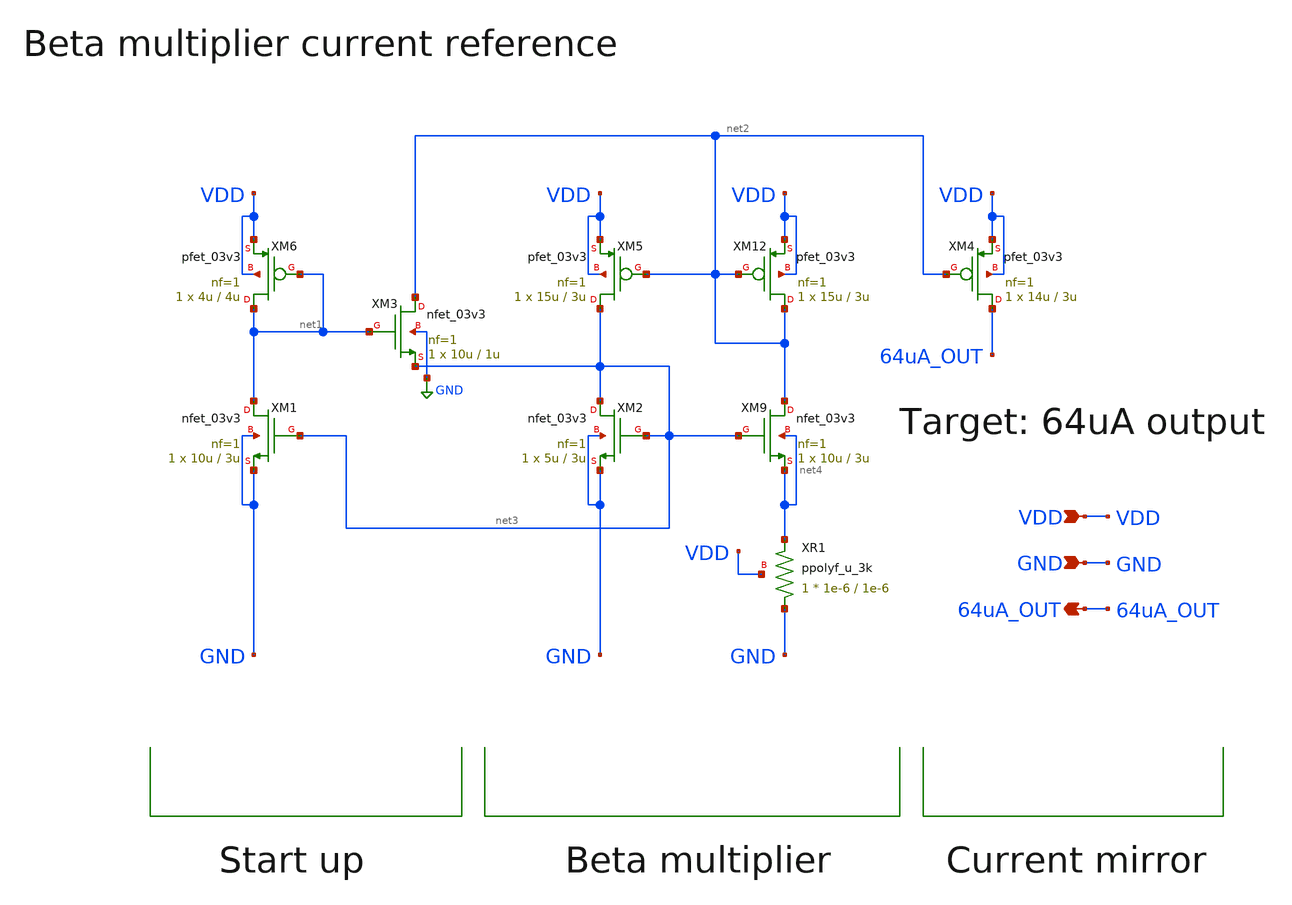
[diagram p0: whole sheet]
** sch_path: designs/libs/core_analog/bmr/bmr.sch
* Copyright 2022 GlobalFoundries PDK Authors
* Licensed under the Apache License, Version 2.0 (the "License");
* you may not use this file except in compliance with the License.
* You may obtain a copy of the License at
* https://www.apache.org/licenses/LICENSE-2.0
* Unless required by applicable law or agreed to in writing, software
* distributed under the License is distributed on an "AS IS" BASIS,
* WITHOUT WARRANTIES OR CONDITIONS OF ANY KIND, either express or implied.
* See the License for the specific language governing permissions and
* limitations under the License.
**.subckt bmr VDD GND 64uA_OUT
*.ipin VDD
*.ipin GND
*.opin 64uA_OUT
XM3 net2 net1 net3 GND nfet_03v3 L=1u W=10u nf=1 ad='int((nf+1)/2) * W/nf * 0.18u' as='int((nf+2)/2) * W/nf * 0.18u'
+ pd='2*int((nf+1)/2) * (W/nf + 0.18u)' ps='2*int((nf+2)/2) * (W/nf + 0.18u)' nrd='0.18u / W' nrs='0.18u / W'
+ sa=0 sb=0 sd=0 m=1
XM5 net3 net2 VDD VDD pfet_03v3 L=3u W=15u nf=1 ad='int((nf+1)/2) * W/nf * 0.18u' as='int((nf+2)/2) * W/nf * 0.18u'
+ pd='2*int((nf+1)/2) * (W/nf + 0.18u)' ps='2*int((nf+2)/2) * (W/nf + 0.18u)' nrd='0.18u / W' nrs='0.18u / W'
+ sa=0 sb=0 sd=0 m=1
XM6 net1 net1 VDD VDD pfet_03v3 L=4u W=4u nf=1 ad='int((nf+1)/2) * W/nf * 0.18u' as='int((nf+2)/2) * W/nf * 0.18u'
+ pd='2*int((nf+1)/2) * (W/nf + 0.18u)' ps='2*int((nf+2)/2) * (W/nf + 0.18u)' nrd='0.18u / W' nrs='0.18u / W'
+ sa=0 sb=0 sd=0 m=1
XM9 net2 net3 net4 net4 nfet_03v3 L=3u W=10u nf=1 ad='int((nf+1)/2) * W/nf * 0.18u' as='int((nf+2)/2) * W/nf * 0.18u'
+ pd='2*int((nf+1)/2) * (W/nf + 0.18u)' ps='2*int((nf+2)/2) * (W/nf + 0.18u)' nrd='0.18u / W' nrs='0.18u / W'
+ sa=0 sb=0 sd=0 m=1
XM12 net2 net2 VDD VDD pfet_03v3 L=3u W=15u nf=1 ad='int((nf+1)/2) * W/nf * 0.18u' as='int((nf+2)/2) * W/nf * 0.18u'
+ pd='2*int((nf+1)/2) * (W/nf + 0.18u)' ps='2*int((nf+2)/2) * (W/nf + 0.18u)' nrd='0.18u / W' nrs='0.18u / W'
+ sa=0 sb=0 sd=0 m=1
XM1 net1 net3 GND GND nfet_03v3 L=3u W=10u nf=1 ad='int((nf+1)/2) * W/nf * 0.18u' as='int((nf+2)/2) * W/nf * 0.18u'
+ pd='2*int((nf+1)/2) * (W/nf + 0.18u)' ps='2*int((nf+2)/2) * (W/nf + 0.18u)' nrd='0.18u / W' nrs='0.18u / W'
+ sa=0 sb=0 sd=0 m=1
XM2 net3 net3 GND GND nfet_03v3 L=3u W=5u nf=1 ad='int((nf+1)/2) * W/nf * 0.18u' as='int((nf+2)/2) * W/nf * 0.18u'
+ pd='2*int((nf+1)/2) * (W/nf + 0.18u)' ps='2*int((nf+2)/2) * (W/nf + 0.18u)' nrd='0.18u / W' nrs='0.18u / W'
+ sa=0 sb=0 sd=0 m=1
XM4 64uA_OUT net2 VDD VDD pfet_03v3 L=3u W=14u nf=1 ad='int((nf+1)/2) * W/nf * 0.18u' as='int((nf+2)/2) * W/nf * 0.18u'
+ pd='2*int((nf+1)/2) * (W/nf + 0.18u)' ps='2*int((nf+2)/2) * (W/nf + 0.18u)' nrd='0.18u / W' nrs='0.18u / W'
+ sa=0 sb=0 sd=0 m=1
XR1 GND net4 VDD ppolyf_u_3k r_width=1e-6 r_length=1e-6 m=1
**.ends
.GLOBAL GND
.end
